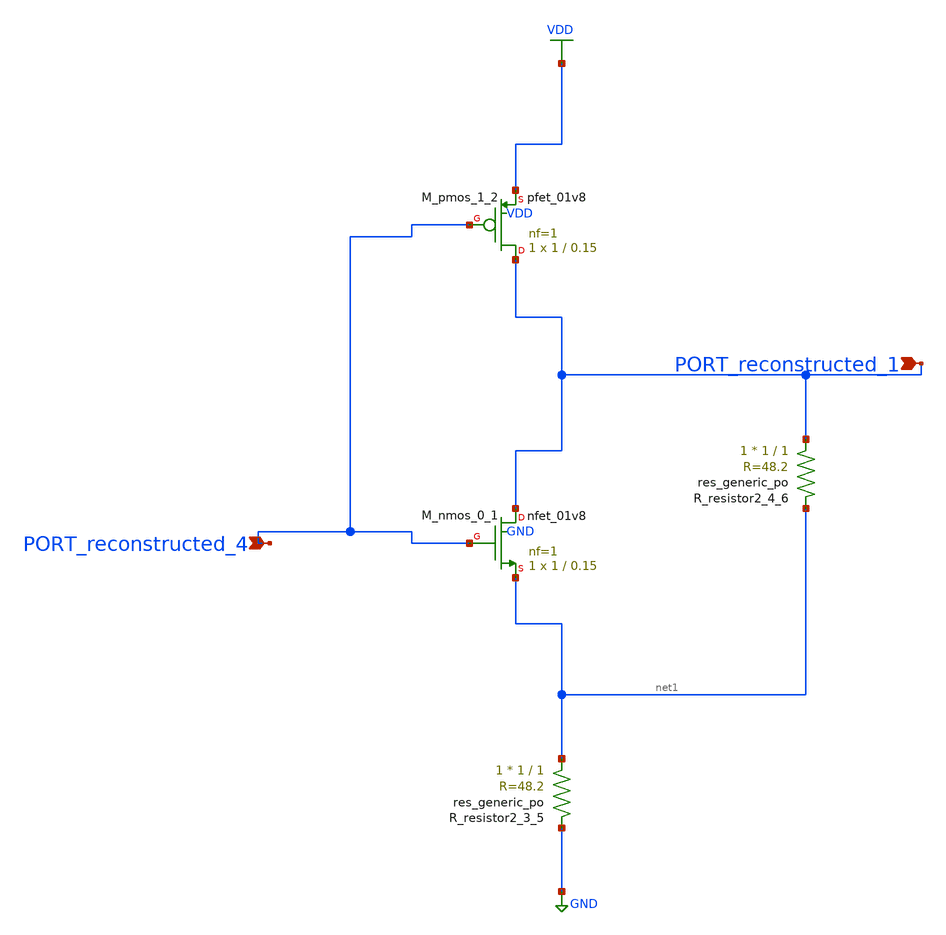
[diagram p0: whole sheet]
** sch_path: schematics/AMSNet/513.sch
**.subckt 513 PORT_reconstructed_4 PORT_reconstructed_1
*.ipin PORT_reconstructed_4
*.ipin PORT_reconstructed_1
XM_nmos_0_1 PORT_reconstructed_1 PORT_reconstructed_4 net1 GND sky130_fd_pr__nfet_01v8 L=0.15 W=1 nf=1
+ ad='int((1 + 1)/2) * 1 / 1 * 0.29' as='int((1 + 2)/2) * 1 / 1 * 0.29' pd='2*int((1 + 1)/2) * (1 / 1 + 0.29)'
+ ps='2*int((1 + 2)/2) * (1 / 1 + 0.29)' nrd='0.29 / 1 ' nrs='0.29 / 1 ' sa=0 sb=0 sd=0 mult=1 m=1
XM_pmos_1_2 PORT_reconstructed_1 PORT_reconstructed_4 VDD VDD sky130_fd_pr__pfet_01v8 L=0.15 W=1 nf=1
+ ad='int((1 + 1)/2) * 1 / 1 * 0.29' as='int((1 + 2)/2) * 1 / 1 * 0.29' pd='2*int((1 + 1)/2) * (1 / 1 + 0.29)'
+ ps='2*int((1 + 2)/2) * (1 / 1 + 0.29)' nrd='0.29 / 1 ' nrs='0.29 / 1 ' sa=0 sb=0 sd=0 mult=1 m=1
XR_resistor2_3_5 net1 GND sky130_fd_pr__res_generic_po W=1 L=1 m=1
XR_resistor2_4_6 PORT_reconstructed_1 net1 sky130_fd_pr__res_generic_po W=1 L=1 m=1
**.ends
.GLOBAL GND
.GLOBAL VDD
.end
